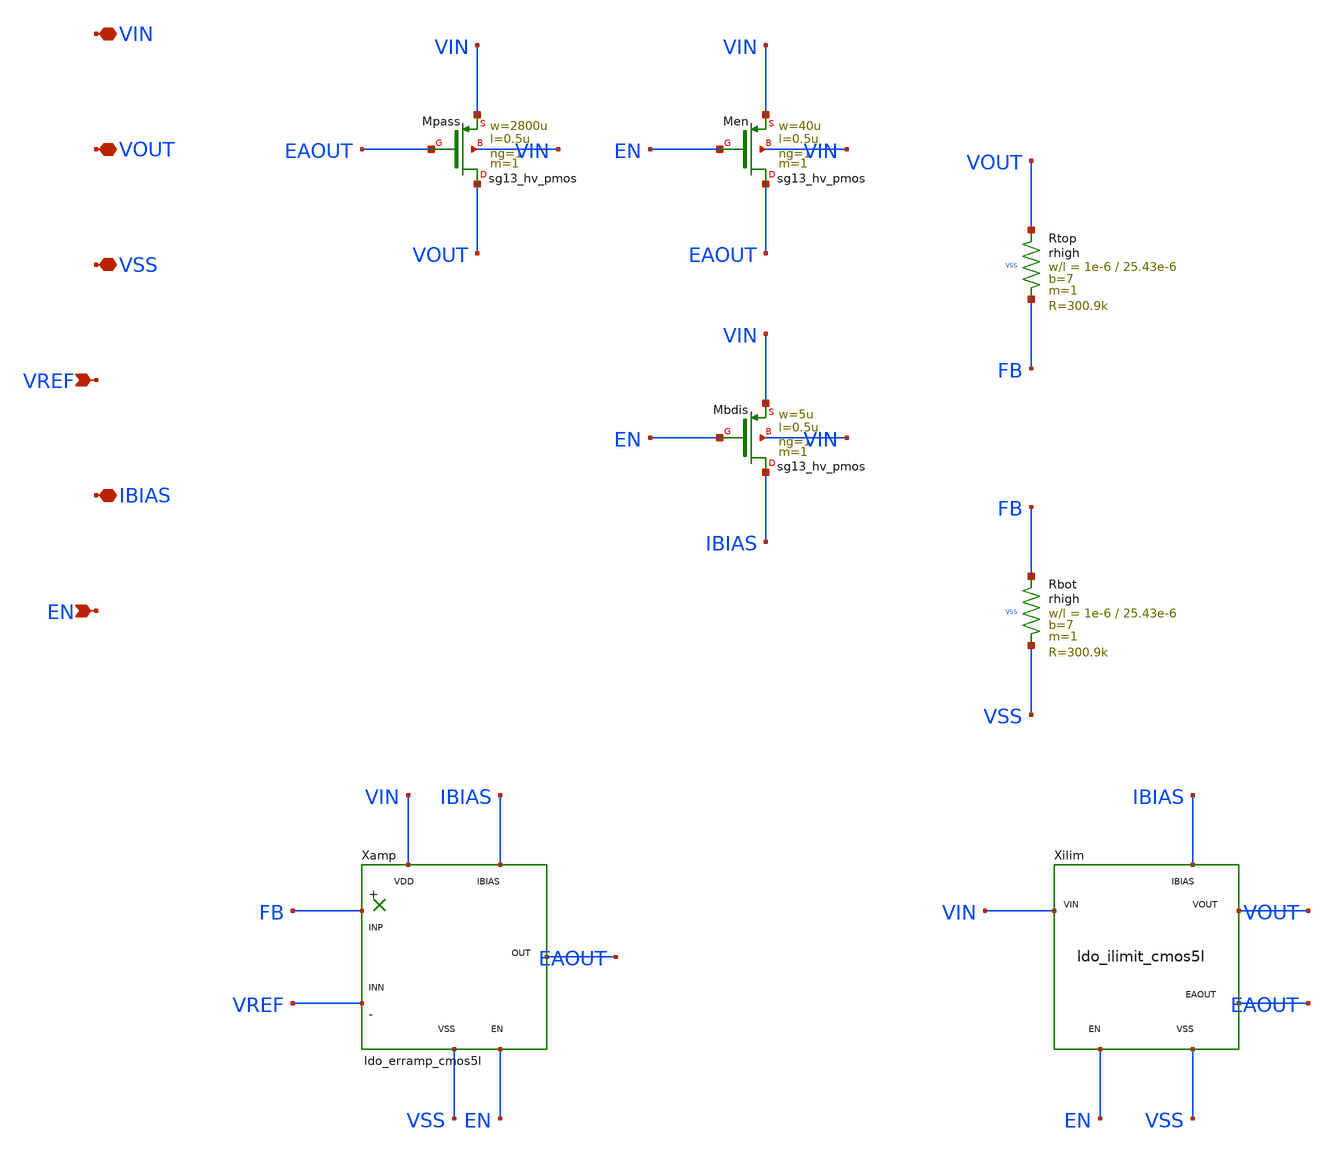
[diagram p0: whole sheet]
** sch_path: design/sg13cmos5l/ldo_core_cmos5l.sch
**.subckt ldo_core_cmos5l VIN VOUT VSS VREF IBIAS EN
*.iopin VIN
*.iopin VOUT
*.iopin VSS
*.ipin VREF
*.iopin IBIAS
*.ipin EN
XMpass VOUT EAOUT VIN VIN sg13_hv_pmos w=2800u l=0.5u ng=1 m=1 mm_ok=1
XRtop VOUT FB VSS rhigh w=1e-6 l=25.43e-6 m=1 b=7 mm_ok=1
XRbot FB VSS VSS rhigh w=1e-6 l=25.43e-6 m=1 b=7 mm_ok=1
Xamp FB VREF EAOUT VIN VSS IBIAS EN ldo_erramp_cmos5l
XMen EAOUT EN VIN VIN sg13_hv_pmos w=40u l=0.5u ng=1 m=1 mm_ok=1
XMbdis IBIAS EN VIN VIN sg13_hv_pmos w=5u l=0.5u ng=1 m=1 mm_ok=1
Xilim VIN VOUT EAOUT IBIAS EN VSS ldo_ilimit_cmos5l
**.ends

* expanding   symbol:  ldo_erramp_cmos5l.sym # of pins=7
** sym_path: design/sg13cmos5l/ldo_erramp_cmos5l.sym
** sch_path: design/sg13cmos5l/ldo_erramp_cmos5l.sch
.subckt ldo_erramp_cmos5l INP INN OUT VDD VSS IBIAS EN
*.ipin INP
*.ipin INN
*.opin OUT
*.iopin VDD
*.iopin VSS
*.iopin IBIAS
*.ipin EN
XMb0 IBIAS IBIAS VDD VDD sg13_hv_pmos w=5u l=2u ng=1 m=1 mm_ok=1
XMtail TAIL IBIAS VDD VDD sg13_hv_pmos w=5u l=2u ng=1 m=3 mm_ok=1
XMload2 OUT IBIAS VDD VDD sg13_hv_pmos w=5u l=2u ng=1 m=6 mm_ok=1
XMinp G1 INP TAIL TAIL sg13_hv_pmos w=20u l=1u ng=1 m=1 mm_ok=1
XMinn N1 INN TAIL TAIL sg13_hv_pmos w=20u l=1u ng=1 m=1 mm_ok=1
XMn2 G1 N1 VSS VSS sg13_hv_nmos w=5u l=1u ng=1 m=1 mm_ok=1
XMn1 N1 N1 VSS VSS sg13_hv_nmos w=5u l=1u ng=1 m=1 mm_ok=1
XMn3 OUT G1 VSS VSS sg13_hv_nmos w=20u l=1u ng=1 m=1 mm_ok=1
XCc OUT MZ cap_cmomi w=170e-6 l=30e-6 mmin=1 mmax=4 feed=double subblock=0 m=1 mm_ok=1
XRz MZ G1 VSS rhigh w=1e-6 l=28.81e-6 m=1 b=39 mm_ok=1
XMinvp ENB EN VDD VDD sg13_hv_pmos w=1u l=1u ng=1 m=1 mm_ok=1
XMinvn ENB EN VSS VSS sg13_hv_nmos w=1u l=1u ng=1 m=1 mm_ok=1
XMpd G1 ENB VSS VSS sg13_hv_nmos w=1u l=1u ng=1 m=1 mm_ok=1
.ends


* expanding   symbol:  ldo_ilimit_cmos5l.sym # of pins=6
** sym_path: design/sg13cmos5l/ldo_ilimit_cmos5l.sym
** sch_path: design/sg13cmos5l/ldo_ilimit_cmos5l.sch
.subckt ldo_ilimit_cmos5l VIN VOUT EAOUT IBIAS EN VSS
*.iopin VIN
*.iopin VOUT
*.iopin EAOUT
*.iopin IBIAS
*.ipin EN
*.iopin VSS
XMsense ISNS EAOUT VIN VIN sg13_hv_pmos w=25u l=0.5u ng=1 m=1 mm_ok=1
XRsns ISNS VOUT VSS rhigh w=2e-6 l=7.09e-6 m=20 b=0 mm_ok=1
XMref1 REFM IBIAS VIN VIN sg13_hv_pmos w=5u l=2u ng=1 m=1 mm_ok=1
XMref2 VTH IBIAS REFM VIN sg13_hv_pmos w=5u l=2u ng=1 m=1 mm_ok=1
XRref1 VTH RN1 VSS rhigh w=2e-6 l=7.09e-6 m=1 b=0 mm_ok=1
XRref2 RN1 RN2 VSS rhigh w=2e-6 l=7.09e-6 m=1 b=0 mm_ok=1
XRref3 RN2 RN3 VSS rhigh w=2e-6 l=7.09e-6 m=1 b=0 mm_ok=1
XRref4 RN3 RN4 VSS rhigh w=2e-6 l=7.09e-6 m=1 b=0 mm_ok=1
XRref5 RN4 RN5 VSS rhigh w=2e-6 l=7.09e-6 m=1 b=0 mm_ok=1
XRref6 RN5 RN6 VSS rhigh w=2e-6 l=7.09e-6 m=1 b=0 mm_ok=1
XRref7 RN6 RN7 VSS rhigh w=2e-6 l=7.09e-6 m=1 b=0 mm_ok=1
XRref8 RN7 RN8 VSS rhigh w=2e-6 l=7.09e-6 m=1 b=0 mm_ok=1
XRref9 RN8 RN9 VSS rhigh w=2e-6 l=7.09e-6 m=1 b=0 mm_ok=1
XRref10 RN9 RN10 VSS rhigh w=2e-6 l=7.09e-6 m=1 b=0 mm_ok=1
XRref11 RN10 RN11 VSS rhigh w=2e-6 l=7.09e-6 m=1 b=0 mm_ok=1
XRref12 RN11 RN12 VSS rhigh w=2e-6 l=7.09e-6 m=1 b=0 mm_ok=1
XRref13 RN12 RN13 VSS rhigh w=2e-6 l=7.09e-6 m=1 b=0 mm_ok=1
XRref14 RN13 RN14 VSS rhigh w=2e-6 l=7.09e-6 m=1 b=0 mm_ok=1
XRref15 RN14 RN15 VSS rhigh w=2e-6 l=7.09e-6 m=1 b=0 mm_ok=1
XRref16 RN15 RN16 VSS rhigh w=2e-6 l=7.09e-6 m=1 b=0 mm_ok=1
XRref17 RN16 RN17 VSS rhigh w=2e-6 l=7.09e-6 m=1 b=0 mm_ok=1
XRref18 RN17 RN18 VSS rhigh w=2e-6 l=7.09e-6 m=1 b=0 mm_ok=1
XRref19 RN18 RN19 VSS rhigh w=2e-6 l=7.09e-6 m=1 b=0 mm_ok=1
XRref20 RN19 RN20 VSS rhigh w=2e-6 l=7.09e-6 m=1 b=0 mm_ok=1
XRref21 RN20 RN21 VSS rhigh w=2e-6 l=7.09e-6 m=1 b=0 mm_ok=1
XRref22 RN21 RN22 VSS rhigh w=2e-6 l=7.09e-6 m=1 b=0 mm_ok=1
XRref23 RN22 RN23 VSS rhigh w=2e-6 l=7.09e-6 m=1 b=0 mm_ok=1
XRref24 RN23 RN24 VSS rhigh w=2e-6 l=7.09e-6 m=1 b=0 mm_ok=1
XRref25 RN24 RN25 VSS rhigh w=2e-6 l=7.09e-6 m=1 b=0 mm_ok=1
XRref26 RN25 RN26 VSS rhigh w=2e-6 l=7.09e-6 m=1 b=0 mm_ok=1
XRref27 RN26 RN27 VSS rhigh w=2e-6 l=7.09e-6 m=1 b=0 mm_ok=1
XRref28 RN27 RN28 VSS rhigh w=2e-6 l=7.09e-6 m=1 b=0 mm_ok=1
XRref29 RN28 RN29 VSS rhigh w=2e-6 l=7.09e-6 m=1 b=0 mm_ok=1
XRref30 RN29 RN30 VSS rhigh w=2e-6 l=7.09e-6 m=1 b=0 mm_ok=1
XRref31 RN30 RN31 VSS rhigh w=2e-6 l=7.09e-6 m=1 b=0 mm_ok=1
XRref32 RN31 VOUT VSS rhigh w=2e-6 l=7.09e-6 m=1 b=0 mm_ok=1
XMca CN ISNS TAIL VIN sg13_hv_pmos w=40u l=2u ng=1 m=1 mm_ok=1
XMcb CO VTH TAIL VIN sg13_hv_pmos w=40u l=2u ng=1 m=1 mm_ok=1
XMna CN CN VSS VSS sg13_hv_nmos w=10u l=8u ng=1 m=1 mm_ok=1
XMnb CO CN VSS VSS sg13_hv_nmos w=10u l=8u ng=1 m=1 mm_ok=1
XRtail TAILP TAIL VSS rhigh w=1e-6 l=26.1e-6 m=1 b=14 mm_ok=1
XMen_t TAILP ENB VIN VIN sg13_hv_pmos w=5u l=0.5u ng=1 m=1 mm_ok=1
XCcl CO VSS cap_cmomi w=22e-6 l=22e-6 mmin=1 mmax=4 feed=double subblock=0 m=1 mm_ok=1
XMen_co CO ENB VSS VSS sg13_hv_nmos w=1u l=1u ng=1 m=1 mm_ok=1
XMg2 CLG CO VSS VSS sg13_hv_nmos w=10u l=1u ng=1 m=1 mm_ok=1
XMlg CLG IBIAS VIN VIN sg13_hv_pmos w=5u l=2u ng=1 m=1 mm_ok=1
XMcoff CLG EN VIN VIN sg13_hv_pmos w=2u l=0.5u ng=1 m=1 mm_ok=1
XMclamp EAOUT CLG VIN VIN sg13_hv_pmos w=40u l=0.5u ng=1 m=1 mm_ok=1
XMinvp ENB EN VIN VIN sg13_hv_pmos w=1u l=1u ng=1 m=1 mm_ok=1
XMinvn ENB EN VSS VSS sg13_hv_nmos w=1u l=1u ng=1 m=1 mm_ok=1
.ends

.end
